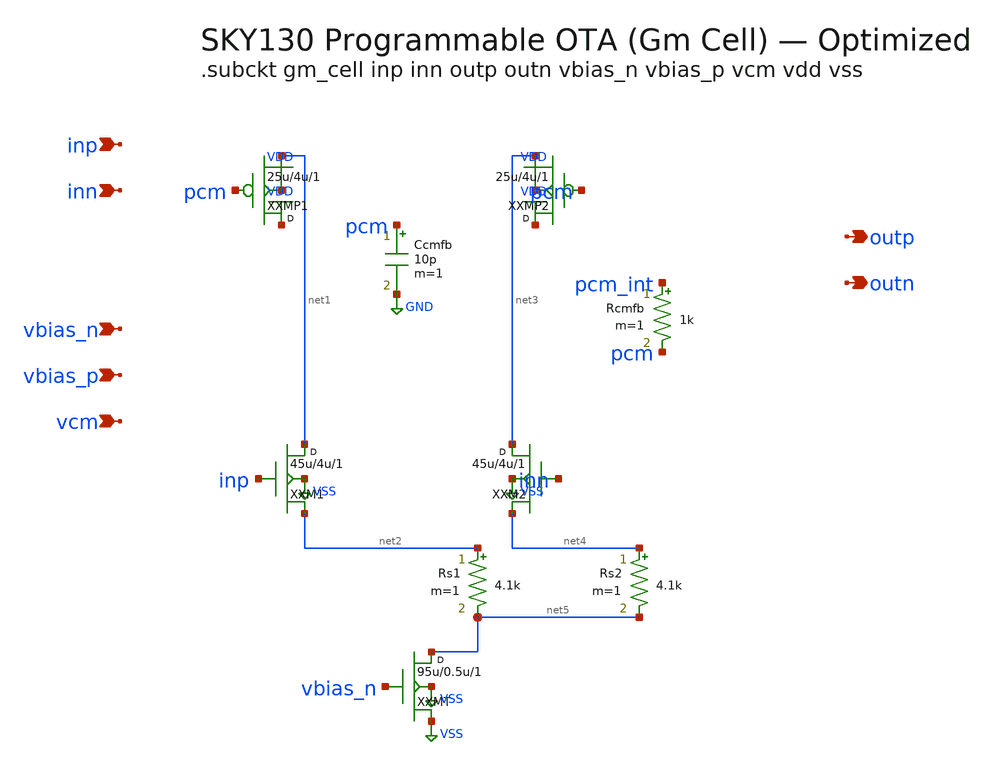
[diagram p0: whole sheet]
** sch_path: data/sch/ode_gm-cell.sch
**.subckt ode_gm-cell inp inn outp outn vbias_n vbias_p vcm
*.ipin inp
*.ipin inn
*.opin outp
*.opin outn
*.ipin vbias_n
*.ipin vbias_p
*.ipin vcm
XXM1 net1 inp net2 VSS sky130_fd_pr__nfet_01v8 w=45u l=4u m=1
XXM2 net3 inn net4 VSS sky130_fd_pr__nfet_01v8 w=45u l=4u m=1
Rs1 net2 net5 4.1k m=1
Rs2 net4 net5 4.1k m=1
XXMT net5 vbias_n VSS VSS sky130_fd_pr__nfet_01v8 w=95u l=0.5u m=1
XXMP1 VDD pcm net1 VDD sky130_fd_pr__pfet_01v8 w=25u l=4u m=1
XXMP2 VDD pcm net3 VDD sky130_fd_pr__pfet_01v8 w=25u l=4u m=1
Rcmfb pcm_int pcm 1k m=1
Ccmfb pcm GND 10p m=1
**.ends
.GLOBAL VSS
.GLOBAL VDD
.GLOBAL GND
.end
